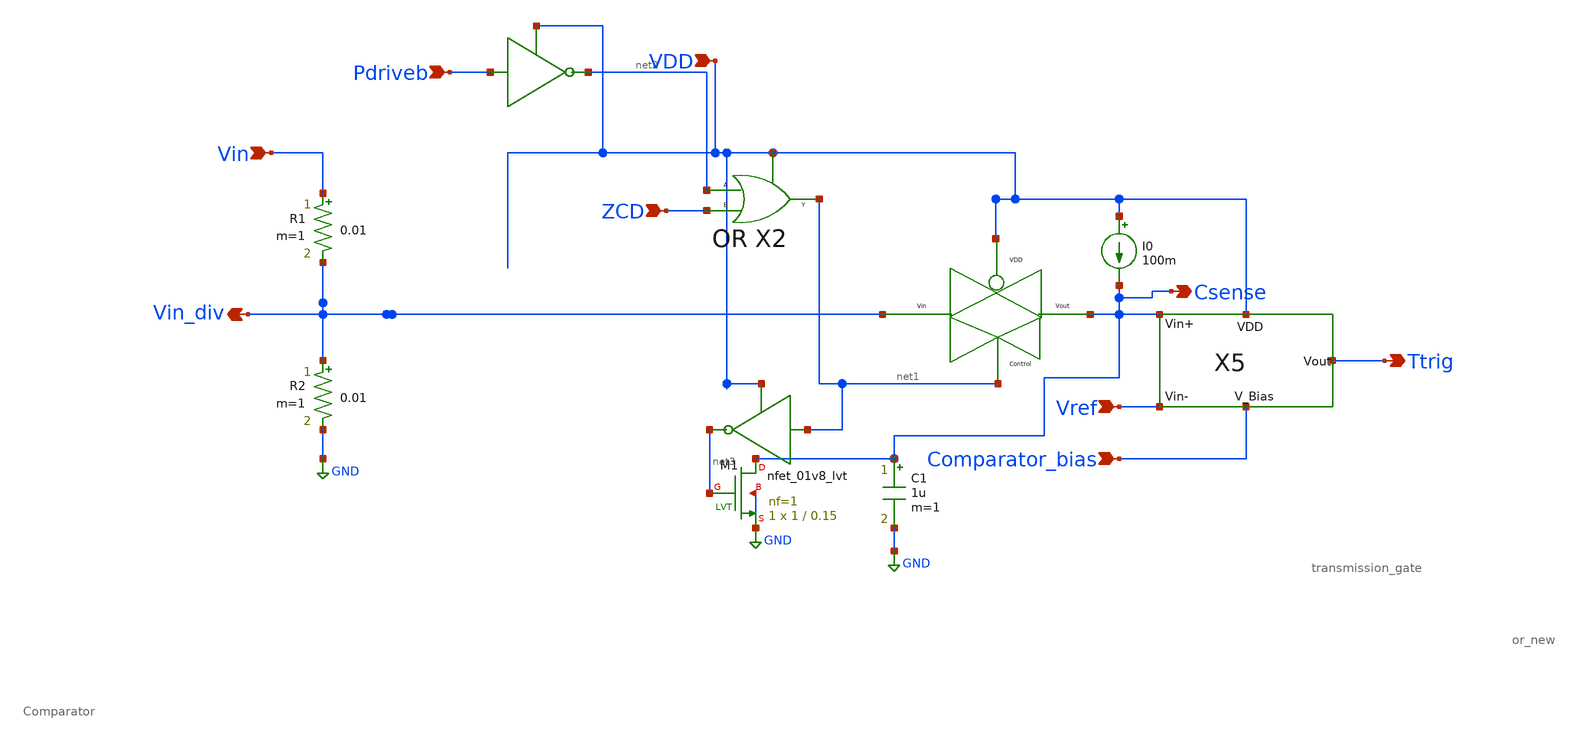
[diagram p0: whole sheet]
** sch_path: Current Sensor/untitled-71.sch
**.subckt untitled-71 Vref Vin_div Comparator_bias Pdriveb ZCD Vin Ttrig VDD Csense
*.ipin Vref
*.opin Vin_div
*.ipin Comparator_bias
*.ipin Pdriveb
*.ipin ZCD
*.ipin Vin
*.opin Ttrig
*.ipin VDD
*.opin Csense
X1 Vin_div Csense net1 VDD transmission_gate
X5 Comparator_bias Csense Vref Ttrig VDD Comparator
R1 Vin Vin_div 0.01 m=1
R2 Vin_div GND 0.01 m=1
C1 Csense GND 1u m=1
X2 ZCD net2 net1 VDD or_new
I0 VDD Csense 100m
XM1 Csense net3 GND GND sky130_fd_pr__nfet_01v8_lvt L=0.15 W=1 nf=1 ad='int((nf+1)/2) * W/nf * 0.29'
+ as='int((nf+2)/2) * W/nf * 0.29' pd='2*int((nf+1)/2) * (W/nf + 0.29)' ps='2*int((nf+2)/2) * (W/nf + 0.29)'
+ nrd='0.29 / W' nrs='0.29 / W' sa=0 sb=0 sd=0 mult=1 m=1
**.ends
.GLOBAL GND
.end
